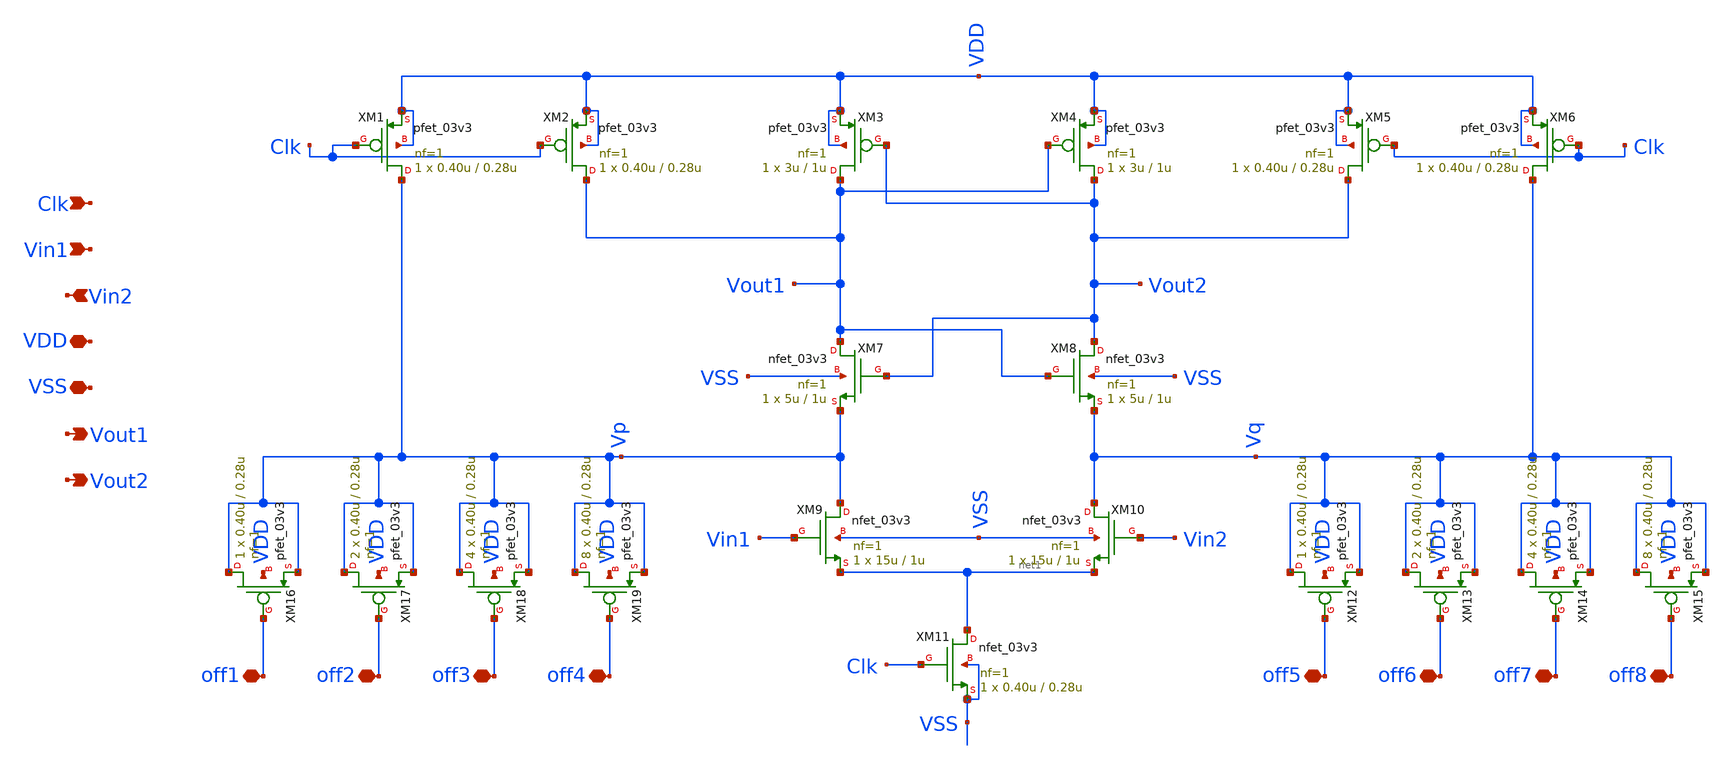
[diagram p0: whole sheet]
** sch_path: designs/comparator/SA_withoffsetcal.sch
**.subckt SA_withoffsetcal Clk Vin1 Vin2 VDD VSS Vout1 Vout2 off5 off6 off7 off8 off1 off2 off3 off4
*.ipin Clk
*.ipin Vin1
*.ipin Vin2
*.iopin VDD
*.iopin VSS
*.opin Vout1
*.opin Vout2
*.iopin off5
*.iopin off6
*.iopin off7
*.iopin off8
*.iopin off1
*.iopin off2
*.iopin off3
*.iopin off4
XM1 Vp Clk VDD VDD pfet_03v3 L=0.28u W=0.40u nf=1 ad='int((nf+1)/2) * W/nf * 0.18u' as='int((nf+2)/2) * W/nf * 0.18u'
+ pd='2*int((nf+1)/2) * (W/nf + 0.18u)' ps='2*int((nf+2)/2) * (W/nf + 0.18u)' nrd='0.18u / W' nrs='0.18u / W'
+ sa=0 sb=0 sd=0 m=1
XM2 Vout1 Clk VDD VDD pfet_03v3 L=0.28u W=0.40u nf=1 ad='int((nf+1)/2) * W/nf * 0.18u' as='int((nf+2)/2) * W/nf * 0.18u'
+ pd='2*int((nf+1)/2) * (W/nf + 0.18u)' ps='2*int((nf+2)/2) * (W/nf + 0.18u)' nrd='0.18u / W' nrs='0.18u / W'
+ sa=0 sb=0 sd=0 m=1
XM3 Vout1 Vout2 VDD VDD pfet_03v3 L=1u W=3u nf=1 ad='int((nf+1)/2) * W/nf * 0.18u' as='int((nf+2)/2) * W/nf * 0.18u'
+ pd='2*int((nf+1)/2) * (W/nf + 0.18u)' ps='2*int((nf+2)/2) * (W/nf + 0.18u)' nrd='0.18u / W' nrs='0.18u / W'
+ sa=0 sb=0 sd=0 m=1
XM4 Vout2 Vout1 VDD VDD pfet_03v3 L=1u W=3u nf=1 ad='int((nf+1)/2) * W/nf * 0.18u' as='int((nf+2)/2) * W/nf * 0.18u'
+ pd='2*int((nf+1)/2) * (W/nf + 0.18u)' ps='2*int((nf+2)/2) * (W/nf + 0.18u)' nrd='0.18u / W' nrs='0.18u / W'
+ sa=0 sb=0 sd=0 m=1
XM5 Vout2 Clk VDD VDD pfet_03v3 L=0.28u W=0.40u nf=1 ad='int((nf+1)/2) * W/nf * 0.18u' as='int((nf+2)/2) * W/nf * 0.18u'
+ pd='2*int((nf+1)/2) * (W/nf + 0.18u)' ps='2*int((nf+2)/2) * (W/nf + 0.18u)' nrd='0.18u / W' nrs='0.18u / W'
+ sa=0 sb=0 sd=0 m=1
XM6 Vq Clk VDD VDD pfet_03v3 L=0.28u W=0.40u nf=1 ad='int((nf+1)/2) * W/nf * 0.18u' as='int((nf+2)/2) * W/nf * 0.18u'
+ pd='2*int((nf+1)/2) * (W/nf + 0.18u)' ps='2*int((nf+2)/2) * (W/nf + 0.18u)' nrd='0.18u / W' nrs='0.18u / W'
+ sa=0 sb=0 sd=0 m=1
XM7 Vout1 Vout2 Vp VSS nfet_03v3 L=1u W=5u nf=1 ad='int((nf+1)/2) * W/nf * 0.18u' as='int((nf+2)/2) * W/nf * 0.18u'
+ pd='2*int((nf+1)/2) * (W/nf + 0.18u)' ps='2*int((nf+2)/2) * (W/nf + 0.18u)' nrd='0.18u / W' nrs='0.18u / W'
+ sa=0 sb=0 sd=0 m=1
XM8 Vout2 Vout1 Vq VSS nfet_03v3 L=1u W=5u nf=1 ad='int((nf+1)/2) * W/nf * 0.18u' as='int((nf+2)/2) * W/nf * 0.18u'
+ pd='2*int((nf+1)/2) * (W/nf + 0.18u)' ps='2*int((nf+2)/2) * (W/nf + 0.18u)' nrd='0.18u / W' nrs='0.18u / W'
+ sa=0 sb=0 sd=0 m=1
XM9 Vp Vin1 net1 VSS nfet_03v3 L=1u W=15u nf=1 ad='int((nf+1)/2) * W/nf * 0.18u' as='int((nf+2)/2) * W/nf * 0.18u'
+ pd='2*int((nf+1)/2) * (W/nf + 0.18u)' ps='2*int((nf+2)/2) * (W/nf + 0.18u)' nrd='0.18u / W' nrs='0.18u / W'
+ sa=0 sb=0 sd=0 m=1
XM10 Vq Vin2 net1 VSS nfet_03v3 L=1u W=15u nf=1 ad='int((nf+1)/2) * W/nf * 0.18u' as='int((nf+2)/2) * W/nf * 0.18u'
+ pd='2*int((nf+1)/2) * (W/nf + 0.18u)' ps='2*int((nf+2)/2) * (W/nf + 0.18u)' nrd='0.18u / W' nrs='0.18u / W'
+ sa=0 sb=0 sd=0 m=1
XM11 net1 Clk VSS VSS nfet_03v3 L=0.28u W=0.40u nf=1 ad='int((nf+1)/2) * W/nf * 0.18u' as='int((nf+2)/2) * W/nf * 0.18u'
+ pd='2*int((nf+1)/2) * (W/nf + 0.18u)' ps='2*int((nf+2)/2) * (W/nf + 0.18u)' nrd='0.18u / W' nrs='0.18u / W'
+ sa=0 sb=0 sd=0 m=1
XM12 Vq off5 Vq VDD pfet_03v3 L=0.28u W=0.40u nf=1 ad='int((nf+1)/2) * W/nf * 0.18u' as='int((nf+2)/2) * W/nf * 0.18u'
+ pd='2*int((nf+1)/2) * (W/nf + 0.18u)' ps='2*int((nf+2)/2) * (W/nf + 0.18u)' nrd='0.18u / W' nrs='0.18u / W'
+ sa=0 sb=0 sd=0 m=1
XM13 Vq off6 Vq VDD pfet_03v3 L=0.28u W=0.40u nf=1 ad='int((nf+1)/2) * W/nf * 0.18u' as='int((nf+2)/2) * W/nf * 0.18u'
+ pd='2*int((nf+1)/2) * (W/nf + 0.18u)' ps='2*int((nf+2)/2) * (W/nf + 0.18u)' nrd='0.18u / W' nrs='0.18u / W'
+ sa=0 sb=0 sd=0 m=2
XM14 Vq off7 Vq VDD pfet_03v3 L=0.28u W=0.40u nf=1 ad='int((nf+1)/2) * W/nf * 0.18u' as='int((nf+2)/2) * W/nf * 0.18u'
+ pd='2*int((nf+1)/2) * (W/nf + 0.18u)' ps='2*int((nf+2)/2) * (W/nf + 0.18u)' nrd='0.18u / W' nrs='0.18u / W'
+ sa=0 sb=0 sd=0 m=4
XM15 Vq off8 Vq VDD pfet_03v3 L=0.28u W=0.40u nf=1 ad='int((nf+1)/2) * W/nf * 0.18u' as='int((nf+2)/2) * W/nf * 0.18u'
+ pd='2*int((nf+1)/2) * (W/nf + 0.18u)' ps='2*int((nf+2)/2) * (W/nf + 0.18u)' nrd='0.18u / W' nrs='0.18u / W'
+ sa=0 sb=0 sd=0 m=8
XM16 Vp off1 Vp VDD pfet_03v3 L=0.28u W=0.40u nf=1 ad='int((nf+1)/2) * W/nf * 0.18u' as='int((nf+2)/2) * W/nf * 0.18u'
+ pd='2*int((nf+1)/2) * (W/nf + 0.18u)' ps='2*int((nf+2)/2) * (W/nf + 0.18u)' nrd='0.18u / W' nrs='0.18u / W'
+ sa=0 sb=0 sd=0 m=1
XM17 Vp off2 Vp VDD pfet_03v3 L=0.28u W=0.40u nf=1 ad='int((nf+1)/2) * W/nf * 0.18u' as='int((nf+2)/2) * W/nf * 0.18u'
+ pd='2*int((nf+1)/2) * (W/nf + 0.18u)' ps='2*int((nf+2)/2) * (W/nf + 0.18u)' nrd='0.18u / W' nrs='0.18u / W'
+ sa=0 sb=0 sd=0 m=2
XM18 Vp off3 Vp VDD pfet_03v3 L=0.28u W=0.40u nf=1 ad='int((nf+1)/2) * W/nf * 0.18u' as='int((nf+2)/2) * W/nf * 0.18u'
+ pd='2*int((nf+1)/2) * (W/nf + 0.18u)' ps='2*int((nf+2)/2) * (W/nf + 0.18u)' nrd='0.18u / W' nrs='0.18u / W'
+ sa=0 sb=0 sd=0 m=4
XM19 Vp off4 Vp VDD pfet_03v3 L=0.28u W=0.40u nf=1 ad='int((nf+1)/2) * W/nf * 0.18u' as='int((nf+2)/2) * W/nf * 0.18u'
+ pd='2*int((nf+1)/2) * (W/nf + 0.18u)' ps='2*int((nf+2)/2) * (W/nf + 0.18u)' nrd='0.18u / W' nrs='0.18u / W'
+ sa=0 sb=0 sd=0 m=8
**.ends
.end
